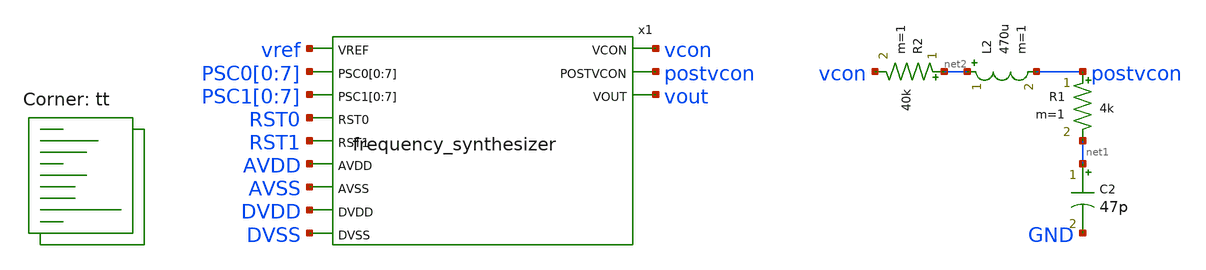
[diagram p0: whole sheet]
** sch_path: xschem/frequency_synthesizer-tb.sch
**.subckt frequency_synthesizer-tb
R1 postvcon net1 4k m=1
R2 net2 vcon 40k m=1
C2 net1 GND 47p m=1
L2 net2 postvcon 470u m=1
x1 vref PSC0[0] PSC0[1] PSC0[2] PSC0[3] PSC0[4] PSC0[5] PSC0[6] PSC0[7] PSC1[0] PSC1[1] PSC1[2]
+ PSC1[3] PSC1[4] PSC1[5] PSC1[6] PSC1[7] RST0 RST1 AVDD AVSS DVDD DVSS vcon postvcon vout
+ frequency_synthesizer
**** begin user architecture code
 .lib $::SKYWATER_MODELS/sky130.lib.spice tt
.include $::SKYWATER_STDCELLS/sky130_fd_sc_hd.spice
.param mc_mm_switch = 0
.param mc_pr_switch = 0




  ***Environtment***
  .include ~/sky130_projects/sky130_its_biomedical_chip_research_2024/spice/freq_psc_8_bit.spice
  .param max_freq=8e6 period={1/max_freq} time_high={period/2}
  .param delay_vin1={time_high} delay_vin2={time_high*1.5}

  .option wnflag=1
  .option safecurrents

  ***Voltage Source***
  Vavdd AVDD AVSS dc 1.8
  Vavss AVSS GND dc 0
  Vdvdd DVDD DVSS dc 1.8
  Vdvss DVSS GND dc 0

  ***Data Signals***
  Vref vref GND pulse(0 1.8 {delay_vin1} 1p 1p {time_high} {period})

  Vrst0  rst0    gnd dc 0
  Vpsc00 psc0[0] gnd dc 1.8
  Vpsc01 psc0[1] gnd dc 1.8
  Vpsc02 psc0[2] gnd dc 1.8
  Vpsc03 psc0[3] gnd dc 0
  Vpsc04 psc0[4] gnd dc 0
  Vpsc05 psc0[5] gnd dc 0
  Vpsc06 psc0[6] gnd dc 0
  Vpsc07 psc0[7] gnd dc 0

  Vrst1  rst1    gnd dc 0
  Vpsc10 psc10[0] gnd dc 1.8
  Vpsc11 psc11[1] gnd dc 1.8
  Vpsc12 psc12[2] gnd dc 1.8
  Vpsc13 psc13[3] gnd dc 0
  Vpsc14 psc14[4] gnd dc 0
  Vpsc15 psc15[5] gnd dc 0
  Vpsc16 psc16[6] gnd dc 0
  Vpsc17 psc17[7] gnd dc 0

  ***Simulation Commands***
  .control
     reset
     save x1.postvref x1.vfeedback x1.up x1.down vcon postvcon vout vref
     +PSC0[0] PSC0[1] PSC0[2] PSC0[3] PSC0[4] PSC0[5] PSC0[6] PSC0[7]
     +PSC1[0] PSC1[1] PSC1[2] PSC1[3] PSC1[4] PSC1[5] PSC1[6] PSC1[7] RST0 RST1
     tran 0.01n 2u uic
     write frequency_synthesizer-tb.raw
    quit 0
  .endc



**** end user architecture code
**.ends

* expanding   symbol:  frequency_synthesizer.sym # of pins=12
** sym_path: xschem/frequency_synthesizer.sym
** sch_path: xschem/frequency_synthesizer.sch
.subckt frequency_synthesizer VREF PSC0[0] PSC0[1] PSC0[2] PSC0[3] PSC0[4] PSC0[5] PSC0[6] PSC0[7]
+ PSC1[0] PSC1[1] PSC1[2] PSC1[3] PSC1[4] PSC1[5] PSC1[6] PSC1[7] RST0 RST1 AVDD AVSS DVDD DVSS VCON POSTVCON
+ VOUT
*.ipin VREF
*.ipin PSC0[0],PSC0[1],PSC0[2],PSC0[3],PSC0[4],PSC0[5],PSC0[6],PSC0[7]
*.ipin PSC1[0],PSC1[1],PSC1[2],PSC1[3],PSC1[4],PSC1[5],PSC1[6],PSC1[7]
*.ipin RST0
*.ipin RST1
*.ipin AVDD
*.ipin AVSS
*.ipin DVDD
*.ipin DVSS
*.opin VCON
*.opin POSTVCON
*.opin VOUT
x1 POSTVREF VFEEDBACK AVDD AVSS DVDD DVSS UP DOWN VCON POSTVCON VOUT pll
x2 DVSS DVDD VREF POSTVREF PSC0[0] PSC0[1] PSC0[2] PSC0[3] PSC0[4] PSC0[5] PSC0[6] PSC0[7] RST0
+ freq_psc_8_bit
x3 DVSS DVDD VOUT VFEEDBACK PSC1[0] PSC1[1] PSC1[2] PSC1[3] PSC1[4] PSC1[5] PSC1[6] PSC1[7] RST1
+ freq_psc_8_bit
.ends


* expanding   symbol:  pll.sym # of pins=11
** sym_path: xschem/pll.sym
** sch_path: xschem/pll.sch
.subckt pll VREF VFEEDBACK AVDD AVSS DVDD DVSS UP DOWN VCON POSTVCON VOUT
*.ipin VREF
*.ipin VFEEDBACK
*.ipin AVDD
*.ipin AVSS
*.ipin DVDD
*.ipin DVSS
*.opin UP
*.opin DOWN
*.opin VCON
*.opin POSTVCON
*.opin VOUT
x1 VREF VFEEDBACK UP DOWN DVDD DVSS pfd
x3 POSTVCON VOUT AVDD AVSS vco
x2 UP DOWN VCON AVDD AVSS DVDD DVSS charge_pump
.ends


* expanding   symbol:  pfd.sym # of pins=6
** sym_path: xschem/pfd.sym
** sch_path: xschem/pfd.sch
.subckt pfd vin1 vin2 U D VDD GND
*.ipin vin1
*.ipin vin2
*.opin U
*.opin D
*.ipin VDD
*.ipin GND
.param wpmos=1.26 lpmos=0.15 wnmos=0.42 lnmos=0.15 wpand=1.5

XM1 net4 rst GND GND sky130_fd_pr__nfet_01v8 L=lnmos W=wnmos nf=1 ad='int((nf+1)/2) * W/nf * 0.29' as='int((nf+2)/2) * W/nf * 0.29'
+ pd='2*int((nf+1)/2) * (W/nf + 0.29)' ps='2*int((nf+2)/2) * (W/nf + 0.29)' nrd='0.29 / W' nrs='0.29 / W'
+ sa=0 sb=0 sd=0 mult=1 m=1
XM2 net3 vin1 VDD VDD sky130_fd_pr__pfet_01v8 L=lpmos W=wpmos nf=1 ad='int((nf+1)/2) * W/nf * 0.29' as='int((nf+2)/2) * W/nf * 0.29'
+ pd='2*int((nf+1)/2) * (W/nf + 0.29)' ps='2*int((nf+2)/2) * (W/nf + 0.29)' nrd='0.29 / W' nrs='0.29 / W'
+ sa=0 sb=0 sd=0 mult=1 m=1
XM3 net4 rst net3 VDD sky130_fd_pr__pfet_01v8 L=lpmos W=wpmos nf=1 ad='int((nf+1)/2) * W/nf * 0.29' as='int((nf+2)/2) * W/nf * 0.29'
+ pd='2*int((nf+1)/2) * (W/nf + 0.29)' ps='2*int((nf+2)/2) * (W/nf + 0.29)' nrd='0.29 / W' nrs='0.29 / W'
+ sa=0 sb=0 sd=0 mult=1 m=1
XM4 net1 net4 VDD VDD sky130_fd_pr__pfet_01v8 L=lpmos W=wpmos nf=1 ad='int((nf+1)/2) * W/nf * 0.29' as='int((nf+2)/2) * W/nf * 0.29'
+ pd='2*int((nf+1)/2) * (W/nf + 0.29)' ps='2*int((nf+2)/2) * (W/nf + 0.29)' nrd='0.29 / W' nrs='0.29 / W'
+ sa=0 sb=0 sd=0 mult=1 m=1
XM5 preU net1 VDD VDD sky130_fd_pr__pfet_01v8 L=lpmos W=wpmos nf=1 ad='int((nf+1)/2) * W/nf * 0.29' as='int((nf+2)/2) * W/nf * 0.29'
+ pd='2*int((nf+1)/2) * (W/nf + 0.29)' ps='2*int((nf+2)/2) * (W/nf + 0.29)' nrd='0.29 / W' nrs='0.29 / W'
+ sa=0 sb=0 sd=0 mult=1 m=1
XM6 net1 net4 net2 GND sky130_fd_pr__nfet_01v8 L=lnmos W=wnmos nf=1 ad='int((nf+1)/2) * W/nf * 0.29'
+ as='int((nf+2)/2) * W/nf * 0.29' pd='2*int((nf+1)/2) * (W/nf + 0.29)' ps='2*int((nf+2)/2) * (W/nf + 0.29)'
+ nrd='0.29 / W' nrs='0.29 / W' sa=0 sb=0 sd=0 mult=1 m=1
XM7 preU net1 GND GND sky130_fd_pr__nfet_01v8 L=lnmos W=wnmos nf=1 ad='int((nf+1)/2) * W/nf * 0.29' as='int((nf+2)/2) * W/nf * 0.29'
+ pd='2*int((nf+1)/2) * (W/nf + 0.29)' ps='2*int((nf+2)/2) * (W/nf + 0.29)' nrd='0.29 / W' nrs='0.29 / W'
+ sa=0 sb=0 sd=0 mult=1 m=1
XM8 net2 vin1 GND GND sky130_fd_pr__nfet_01v8 L=lnmos W=wnmos nf=1 ad='int((nf+1)/2) * W/nf * 0.29' as='int((nf+2)/2) * W/nf * 0.29'
+ pd='2*int((nf+1)/2) * (W/nf + 0.29)' ps='2*int((nf+2)/2) * (W/nf + 0.29)' nrd='0.29 / W' nrs='0.29 / W'
+ sa=0 sb=0 sd=0 mult=1 m=1
XM10 net6 vin2 VDD VDD sky130_fd_pr__pfet_01v8 L=lpmos W=wpmos nf=1 ad='int((nf+1)/2) * W/nf * 0.29'
+ as='int((nf+2)/2) * W/nf * 0.29' pd='2*int((nf+1)/2) * (W/nf + 0.29)' ps='2*int((nf+2)/2) * (W/nf + 0.29)'
+ nrd='0.29 / W' nrs='0.29 / W' sa=0 sb=0 sd=0 mult=1 m=1
XM11 net5 net7 VDD VDD sky130_fd_pr__pfet_01v8 L=lpmos W=wpmos nf=1 ad='int((nf+1)/2) * W/nf * 0.29'
+ as='int((nf+2)/2) * W/nf * 0.29' pd='2*int((nf+1)/2) * (W/nf + 0.29)' ps='2*int((nf+2)/2) * (W/nf + 0.29)'
+ nrd='0.29 / W' nrs='0.29 / W' sa=0 sb=0 sd=0 mult=1 m=1
XM12 net7 rst net6 VDD sky130_fd_pr__pfet_01v8 L=lpmos W=wpmos nf=1 ad='int((nf+1)/2) * W/nf * 0.29'
+ as='int((nf+2)/2) * W/nf * 0.29' pd='2*int((nf+1)/2) * (W/nf + 0.29)' ps='2*int((nf+2)/2) * (W/nf + 0.29)'
+ nrd='0.29 / W' nrs='0.29 / W' sa=0 sb=0 sd=0 mult=1 m=1
XM13 preD net5 VDD VDD sky130_fd_pr__pfet_01v8 L=lpmos W=wpmos nf=1 ad='int((nf+1)/2) * W/nf * 0.29'
+ as='int((nf+2)/2) * W/nf * 0.29' pd='2*int((nf+1)/2) * (W/nf + 0.29)' ps='2*int((nf+2)/2) * (W/nf + 0.29)'
+ nrd='0.29 / W' nrs='0.29 / W' sa=0 sb=0 sd=0 mult=1 m=1
XM14 net7 rst GND GND sky130_fd_pr__nfet_01v8 L=lnmos W=wnmos nf=1 ad='int((nf+1)/2) * W/nf * 0.29' as='int((nf+2)/2) * W/nf * 0.29'
+ pd='2*int((nf+1)/2) * (W/nf + 0.29)' ps='2*int((nf+2)/2) * (W/nf + 0.29)' nrd='0.29 / W' nrs='0.29 / W'
+ sa=0 sb=0 sd=0 mult=1 m=1
XM15 net5 net7 net8 GND sky130_fd_pr__nfet_01v8 L=lnmos W=wnmos nf=1 ad='int((nf+1)/2) * W/nf * 0.29'
+ as='int((nf+2)/2) * W/nf * 0.29' pd='2*int((nf+1)/2) * (W/nf + 0.29)' ps='2*int((nf+2)/2) * (W/nf + 0.29)'
+ nrd='0.29 / W' nrs='0.29 / W' sa=0 sb=0 sd=0 mult=1 m=1
XM16 preD net5 GND GND sky130_fd_pr__nfet_01v8 L=lnmos W=wnmos nf=1 ad='int((nf+1)/2) * W/nf * 0.29'
+ as='int((nf+2)/2) * W/nf * 0.29' pd='2*int((nf+1)/2) * (W/nf + 0.29)' ps='2*int((nf+2)/2) * (W/nf + 0.29)'
+ nrd='0.29 / W' nrs='0.29 / W' sa=0 sb=0 sd=0 mult=1 m=1
XM18 net8 vin2 GND GND sky130_fd_pr__nfet_01v8 L=lnmos W=wnmos nf=1 ad='int((nf+1)/2) * W/nf * 0.29'
+ as='int((nf+2)/2) * W/nf * 0.29' pd='2*int((nf+1)/2) * (W/nf + 0.29)' ps='2*int((nf+2)/2) * (W/nf + 0.29)'
+ nrd='0.29 / W' nrs='0.29 / W' sa=0 sb=0 sd=0 mult=1 m=1
x1 preU GND GND VDD VDD U sky130_fd_sc_hd__buf_8
x2 preD GND GND VDD VDD D sky130_fd_sc_hd__buf_8
x3 prerst GND GND VDD VDD rst sky130_fd_sc_hd__buf_1
x4 U D GND GND VDD VDD prerst sky130_fd_sc_hd__and2_1
.ends


* expanding   symbol:  vco.sym # of pins=4
** sym_path: xschem/vco.sym
** sch_path: xschem/vco.sch
.subckt vco VCON VOUT AVDD AVSS
*.ipin VCON
*.opin VOUT
*.ipin AVDD
*.ipin AVSS
.param wpo=4.8 lpo=0.54 wno=2.4 lno=0.54 wpcb=4.8 lpcb=0.36 wncb=0.96 lncb=0.36 wpvb=6 lpvb=0.9
+ wnvc=96 lnvc=0.9 wpbuff=4.8 lpbuff=0.18 wnbuff=1.2 lnbuff=0.18 lres=3.5

XM1 vnbias vnbias AVSS AVSS sky130_fd_pr__nfet_01v8 L=lncb W=wncb nf=1 ad='int((nf+1)/2) * W/nf * 0.29'
+ as='int((nf+2)/2) * W/nf * 0.29' pd='2*int((nf+1)/2) * (W/nf + 0.29)' ps='2*int((nf+2)/2) * (W/nf + 0.29)'
+ nrd='0.29 / W' nrs='0.29 / W' sa=0 sb=0 sd=0 mult=1 m=1
XM2 vpbias vpbias AVDD AVDD sky130_fd_pr__pfet_01v8 L=lpvb W=wpvb nf=1 ad='int((nf+1)/2) * W/nf * 0.29'
+ as='int((nf+2)/2) * W/nf * 0.29' pd='2*int((nf+1)/2) * (W/nf + 0.29)' ps='2*int((nf+2)/2) * (W/nf + 0.29)'
+ nrd='0.29 / W' nrs='0.29 / W' sa=0 sb=0 sd=0 mult=1 m=1
XM4 vnbias vpbias AVDD AVDD sky130_fd_pr__pfet_01v8 L=lpcb W=wpcb nf=1 ad='int((nf+1)/2) * W/nf * 0.29'
+ as='int((nf+2)/2) * W/nf * 0.29' pd='2*int((nf+1)/2) * (W/nf + 0.29)' ps='2*int((nf+2)/2) * (W/nf + 0.29)'
+ nrd='0.29 / W' nrs='0.29 / W' sa=0 sb=0 sd=0 mult=1 m=1
XM5 net8 net9 net1 AVSS sky130_fd_pr__nfet_01v8 L=lno W=wno nf=1 ad='int((nf+1)/2) * W/nf * 0.29' as='int((nf+2)/2) * W/nf * 0.29'
+ pd='2*int((nf+1)/2) * (W/nf + 0.29)' ps='2*int((nf+2)/2) * (W/nf + 0.29)' nrd='0.29 / W' nrs='0.29 / W'
+ sa=0 sb=0 sd=0 mult=1 m=1
XM6 net8 net9 net12 AVDD sky130_fd_pr__pfet_01v8 L=lpo W=wpo nf=1 ad='int((nf+1)/2) * W/nf * 0.29' as='int((nf+2)/2) * W/nf * 0.29'
+ pd='2*int((nf+1)/2) * (W/nf + 0.29)' ps='2*int((nf+2)/2) * (W/nf + 0.29)' nrd='0.29 / W' nrs='0.29 / W'
+ sa=0 sb=0 sd=0 mult=1 m=1
XM7 net7 net8 net2 AVSS sky130_fd_pr__nfet_01v8 L=lno W=wno nf=1 ad='int((nf+1)/2) * W/nf * 0.29' as='int((nf+2)/2) * W/nf * 0.29'
+ pd='2*int((nf+1)/2) * (W/nf + 0.29)' ps='2*int((nf+2)/2) * (W/nf + 0.29)' nrd='0.29 / W' nrs='0.29 / W'
+ sa=0 sb=0 sd=0 mult=1 m=1
XM8 net7 net8 net13 AVDD sky130_fd_pr__pfet_01v8 L=lpo W=wpo nf=1 ad='int((nf+1)/2) * W/nf * 0.29' as='int((nf+2)/2) * W/nf * 0.29'
+ pd='2*int((nf+1)/2) * (W/nf + 0.29)' ps='2*int((nf+2)/2) * (W/nf + 0.29)' nrd='0.29 / W' nrs='0.29 / W'
+ sa=0 sb=0 sd=0 mult=1 m=1
XM9 net6 net7 net3 AVSS sky130_fd_pr__nfet_01v8 L=lno W=wno nf=1 ad='int((nf+1)/2) * W/nf * 0.29' as='int((nf+2)/2) * W/nf * 0.29'
+ pd='2*int((nf+1)/2) * (W/nf + 0.29)' ps='2*int((nf+2)/2) * (W/nf + 0.29)' nrd='0.29 / W' nrs='0.29 / W'
+ sa=0 sb=0 sd=0 mult=1 m=1
XM10 net6 net7 net14 AVDD sky130_fd_pr__pfet_01v8 L=lpo W=wpo nf=1 ad='int((nf+1)/2) * W/nf * 0.29' as='int((nf+2)/2) * W/nf * 0.29'
+ pd='2*int((nf+1)/2) * (W/nf + 0.29)' ps='2*int((nf+2)/2) * (W/nf + 0.29)' nrd='0.29 / W' nrs='0.29 / W'
+ sa=0 sb=0 sd=0 mult=1 m=1
XM11 net10 net6 net5 AVSS sky130_fd_pr__nfet_01v8 L=lno W=wno nf=1 ad='int((nf+1)/2) * W/nf * 0.29' as='int((nf+2)/2) * W/nf * 0.29'
+ pd='2*int((nf+1)/2) * (W/nf + 0.29)' ps='2*int((nf+2)/2) * (W/nf + 0.29)' nrd='0.29 / W' nrs='0.29 / W'
+ sa=0 sb=0 sd=0 mult=1 m=1
XM12 net10 net6 net15 AVDD sky130_fd_pr__pfet_01v8 L=lpo W=wpo nf=1 ad='int((nf+1)/2) * W/nf * 0.29'
+ as='int((nf+2)/2) * W/nf * 0.29' pd='2*int((nf+1)/2) * (W/nf + 0.29)' ps='2*int((nf+2)/2) * (W/nf + 0.29)'
+ nrd='0.29 / W' nrs='0.29 / W' sa=0 sb=0 sd=0 mult=1 m=1
XM13 net9 net10 net4 AVSS sky130_fd_pr__nfet_01v8 L=lno W=wno nf=1 ad='int((nf+1)/2) * W/nf * 0.29' as='int((nf+2)/2) * W/nf * 0.29'
+ pd='2*int((nf+1)/2) * (W/nf + 0.29)' ps='2*int((nf+2)/2) * (W/nf + 0.29)' nrd='0.29 / W' nrs='0.29 / W'
+ sa=0 sb=0 sd=0 mult=1 m=1
XM14 net9 net10 net16 AVDD sky130_fd_pr__pfet_01v8 L=lpo W=wpo nf=1 ad='int((nf+1)/2) * W/nf * 0.29'
+ as='int((nf+2)/2) * W/nf * 0.29' pd='2*int((nf+1)/2) * (W/nf + 0.29)' ps='2*int((nf+2)/2) * (W/nf + 0.29)'
+ nrd='0.29 / W' nrs='0.29 / W' sa=0 sb=0 sd=0 mult=1 m=1
XM16 net12 vpbias AVDD AVDD sky130_fd_pr__pfet_01v8 L=lpcb W=wpcb nf=1 ad='int((nf+1)/2) * W/nf * 0.29'
+ as='int((nf+2)/2) * W/nf * 0.29' pd='2*int((nf+1)/2) * (W/nf + 0.29)' ps='2*int((nf+2)/2) * (W/nf + 0.29)'
+ nrd='0.29 / W' nrs='0.29 / W' sa=0 sb=0 sd=0 mult=1 m=1
XM18 net13 vpbias AVDD AVDD sky130_fd_pr__pfet_01v8 L=lpcb W=wpcb nf=1 ad='int((nf+1)/2) * W/nf * 0.29'
+ as='int((nf+2)/2) * W/nf * 0.29' pd='2*int((nf+1)/2) * (W/nf + 0.29)' ps='2*int((nf+2)/2) * (W/nf + 0.29)'
+ nrd='0.29 / W' nrs='0.29 / W' sa=0 sb=0 sd=0 mult=1 m=1
XM20 net14 vpbias AVDD AVDD sky130_fd_pr__pfet_01v8 L=lpcb W=wpcb nf=1 ad='int((nf+1)/2) * W/nf * 0.29'
+ as='int((nf+2)/2) * W/nf * 0.29' pd='2*int((nf+1)/2) * (W/nf + 0.29)' ps='2*int((nf+2)/2) * (W/nf + 0.29)'
+ nrd='0.29 / W' nrs='0.29 / W' sa=0 sb=0 sd=0 mult=1 m=1
XM22 net15 vpbias AVDD AVDD sky130_fd_pr__pfet_01v8 L=lpcb W=wpcb nf=1 ad='int((nf+1)/2) * W/nf * 0.29'
+ as='int((nf+2)/2) * W/nf * 0.29' pd='2*int((nf+1)/2) * (W/nf + 0.29)' ps='2*int((nf+2)/2) * (W/nf + 0.29)'
+ nrd='0.29 / W' nrs='0.29 / W' sa=0 sb=0 sd=0 mult=1 m=1
XM24 net16 vpbias AVDD AVDD sky130_fd_pr__pfet_01v8 L=lpcb W=wpcb nf=1 ad='int((nf+1)/2) * W/nf * 0.29'
+ as='int((nf+2)/2) * W/nf * 0.29' pd='2*int((nf+1)/2) * (W/nf + 0.29)' ps='2*int((nf+2)/2) * (W/nf + 0.29)'
+ nrd='0.29 / W' nrs='0.29 / W' sa=0 sb=0 sd=0 mult=1 m=1
XM25 net11 net9 AVSS AVSS sky130_fd_pr__nfet_01v8 L=lnbuff W=wnbuff nf=1 ad='int((nf+1)/2) * W/nf * 0.29'
+ as='int((nf+2)/2) * W/nf * 0.29' pd='2*int((nf+1)/2) * (W/nf + 0.29)' ps='2*int((nf+2)/2) * (W/nf + 0.29)'
+ nrd='0.29 / W' nrs='0.29 / W' sa=0 sb=0 sd=0 mult=1 m=1
XM26 net11 net9 AVDD AVDD sky130_fd_pr__pfet_01v8 L=lpbuff W=wpbuff nf=1 ad='int((nf+1)/2) * W/nf * 0.29'
+ as='int((nf+2)/2) * W/nf * 0.29' pd='2*int((nf+1)/2) * (W/nf + 0.29)' ps='2*int((nf+2)/2) * (W/nf + 0.29)'
+ nrd='0.29 / W' nrs='0.29 / W' sa=0 sb=0 sd=0 mult=1 m=1
XM27 VOUT net11 AVSS AVSS sky130_fd_pr__nfet_01v8 L=lnbuff W=wnbuff nf=1 ad='int((nf+1)/2) * W/nf * 0.29'
+ as='int((nf+2)/2) * W/nf * 0.29' pd='2*int((nf+1)/2) * (W/nf + 0.29)' ps='2*int((nf+2)/2) * (W/nf + 0.29)'
+ nrd='0.29 / W' nrs='0.29 / W' sa=0 sb=0 sd=0 mult=1 m=1
XM28 VOUT net11 AVDD AVDD sky130_fd_pr__pfet_01v8 L=lpbuff W=wpbuff nf=1 ad='int((nf+1)/2) * W/nf * 0.29'
+ as='int((nf+2)/2) * W/nf * 0.29' pd='2*int((nf+1)/2) * (W/nf + 0.29)' ps='2*int((nf+2)/2) * (W/nf + 0.29)'
+ nrd='0.29 / W' nrs='0.29 / W' sa=0 sb=0 sd=0 mult=1 m=1
XM15 net1 vnbias AVSS AVSS sky130_fd_pr__nfet_01v8 L=lncb W=wncb nf=1 ad='int((nf+1)/2) * W/nf * 0.29'
+ as='int((nf+2)/2) * W/nf * 0.29' pd='2*int((nf+1)/2) * (W/nf + 0.29)' ps='2*int((nf+2)/2) * (W/nf + 0.29)'
+ nrd='0.29 / W' nrs='0.29 / W' sa=0 sb=0 sd=0 mult=1 m=1
XM17 net2 vnbias AVSS AVSS sky130_fd_pr__nfet_01v8 L=lncb W=wncb nf=1 ad='int((nf+1)/2) * W/nf * 0.29'
+ as='int((nf+2)/2) * W/nf * 0.29' pd='2*int((nf+1)/2) * (W/nf + 0.29)' ps='2*int((nf+2)/2) * (W/nf + 0.29)'
+ nrd='0.29 / W' nrs='0.29 / W' sa=0 sb=0 sd=0 mult=1 m=1
XM19 net3 vnbias AVSS AVSS sky130_fd_pr__nfet_01v8 L=lncb W=wncb nf=1 ad='int((nf+1)/2) * W/nf * 0.29'
+ as='int((nf+2)/2) * W/nf * 0.29' pd='2*int((nf+1)/2) * (W/nf + 0.29)' ps='2*int((nf+2)/2) * (W/nf + 0.29)'
+ nrd='0.29 / W' nrs='0.29 / W' sa=0 sb=0 sd=0 mult=1 m=1
XM21 net5 vnbias AVSS AVSS sky130_fd_pr__nfet_01v8 L=lncb W=wncb nf=1 ad='int((nf+1)/2) * W/nf * 0.29'
+ as='int((nf+2)/2) * W/nf * 0.29' pd='2*int((nf+1)/2) * (W/nf + 0.29)' ps='2*int((nf+2)/2) * (W/nf + 0.29)'
+ nrd='0.29 / W' nrs='0.29 / W' sa=0 sb=0 sd=0 mult=1 m=1
XM23 net4 vnbias AVSS AVSS sky130_fd_pr__nfet_01v8 L=lncb W=wncb nf=1 ad='int((nf+1)/2) * W/nf * 0.29'
+ as='int((nf+2)/2) * W/nf * 0.29' pd='2*int((nf+1)/2) * (W/nf + 0.29)' ps='2*int((nf+2)/2) * (W/nf + 0.29)'
+ nrd='0.29 / W' nrs='0.29 / W' sa=0 sb=0 sd=0 mult=1 m=1
XR3 AVSS net17 AVSS sky130_fd_pr__res_xhigh_po W=0.35 L=lres mult=1 m=1
XM29 vpbias VCON net17 AVSS sky130_fd_pr__nfet_01v8 L=lnvc W=wnvc nf=1 ad='int((nf+1)/2) * W/nf * 0.29'
+ as='int((nf+2)/2) * W/nf * 0.29' pd='2*int((nf+1)/2) * (W/nf + 0.29)' ps='2*int((nf+2)/2) * (W/nf + 0.29)'
+ nrd='0.29 / W' nrs='0.29 / W' sa=0 sb=0 sd=0 mult=1 m=1
.ends


* expanding   symbol:  charge_pump.sym # of pins=7
** sym_path: xschem/charge_pump.sym
** sch_path: xschem/charge_pump.sch
.subckt charge_pump U D vcon AVDD AVSS DVDD DVSS
*.ipin U
*.ipin D
*.opin vcon
*.ipin AVDD
*.ipin AVSS
*.ipin DVDD
*.ipin DVSS
XM1 vcon Ub AVDD AVDD sky130_fd_pr__pfet_01v8 L=lmos W=wpmos nf=1 ad='int((nf+1)/2) * W/nf * 0.29' as='int((nf+2)/2) * W/nf * 0.29'
+ pd='2*int((nf+1)/2) * (W/nf + 0.29)' ps='2*int((nf+2)/2) * (W/nf + 0.29)' nrd='0.29 / W' nrs='0.29 / W'
+ sa=0 sb=0 sd=0 mult=4 m=4
XM2 vcon net1 AVSS AVSS sky130_fd_pr__nfet_01v8 L=lmos W=wnmos nf=1 ad='int((nf+1)/2) * W/nf * 0.29'
+ as='int((nf+2)/2) * W/nf * 0.29' pd='2*int((nf+1)/2) * (W/nf + 0.29)' ps='2*int((nf+2)/2) * (W/nf + 0.29)'
+ nrd='0.29 / W' nrs='0.29 / W' sa=0 sb=0 sd=0 mult=4 m=4
.param wpmos=2.5 wnmos=2.5 lmos=1.2
x1 D DVSS DVSS DVDD DVDD net1 sky130_fd_sc_hd__buf_8
x2 U DVSS DVSS DVDD DVDD Ub sky130_fd_sc_hd__inv_8
.ends

.end
